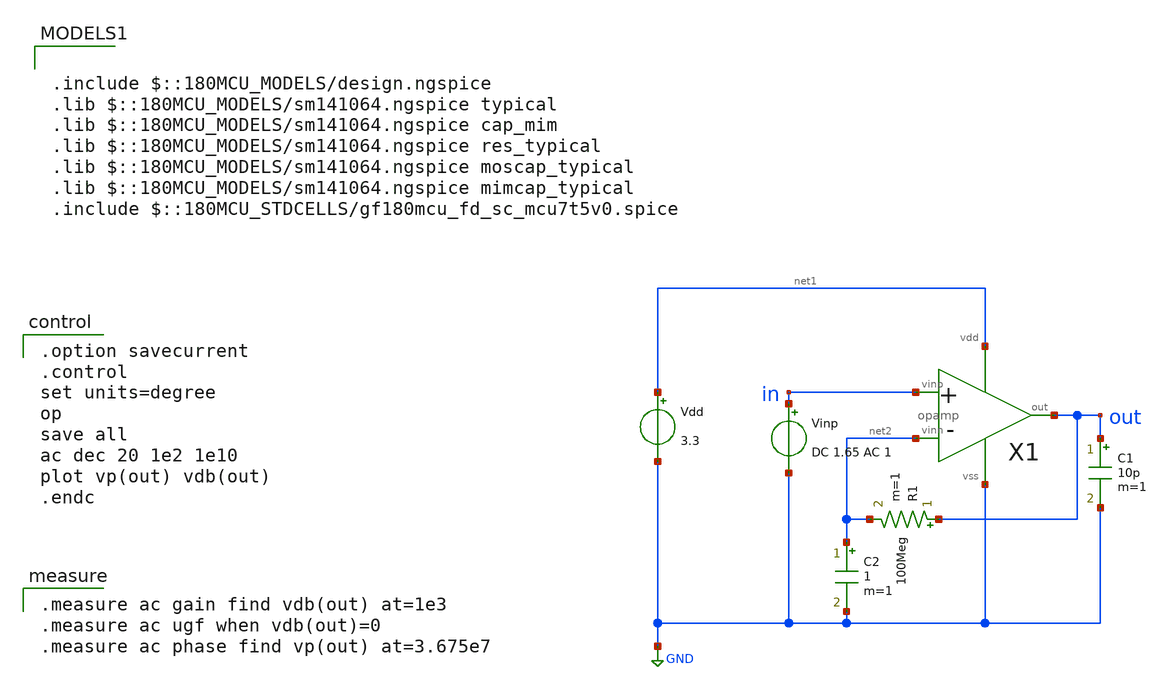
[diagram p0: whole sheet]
** sch_path: opamp_ac.sch
**.subckt opamp_ac
Vdd net1 GND 3.3
Vinp in GND DC 1.65 AC 1
X1 in net2 out net1 GND opamp
R1 out net2 100Meg m=1
C2 net2 GND 1 m=1
C1 out GND 10p m=1
**** begin user architecture code

.option savecurrent
.control
set units=degree
op
save all
ac dec 20 1e2 1e10
plot vp(out) vdb(out)
.endc


.measure ac gain find vdb(out) at=1e3
.measure ac ugf when vdb(out)=0
.measure ac phase find vp(out) at=3.675e7


.include $::180MCU_MODELS/design.ngspice
.lib $::180MCU_MODELS/sm141064.ngspice typical
.lib $::180MCU_MODELS/sm141064.ngspice cap_mim
.lib $::180MCU_MODELS/sm141064.ngspice res_typical
.lib $::180MCU_MODELS/sm141064.ngspice moscap_typical
.lib $::180MCU_MODELS/sm141064.ngspice mimcap_typical
.include $::180MCU_STDCELLS/gf180mcu_fd_sc_mcu7t5v0.spice

**** end user architecture code
**.ends

* expanding   symbol:  opamp.sym # of pins=5
** sym_path: opamp.sym
** sch_path: opamp.sch
.subckt opamp vinp vinn out vdd vss
*.opin out
*.iopin vdd
*.iopin vss
*.ipin vinp
*.ipin vinn
XM2 net2 net1 vdd vdd pfet_03v3 L=0.6u W=6.0u nf=1 ad='int((nf+1)/2) * W/nf * 0.18u' as='int((nf+2)/2) * W/nf * 0.18u'
+ pd='2*int((nf+1)/2) * (W/nf + 0.18u)' ps='2*int((nf+2)/2) * (W/nf + 0.18u)' nrd='0.18u / W' nrs='0.18u / W'
+ sa=0 sb=0 sd=0 m=1
XM3 net1 net3 net2 vdd pfet_03v3 L=0.6u W=6.0u nf=1 ad='int((nf+1)/2) * W/nf * 0.18u' as='int((nf+2)/2) * W/nf * 0.18u'
+ pd='2*int((nf+1)/2) * (W/nf + 0.18u)' ps='2*int((nf+2)/2) * (W/nf + 0.18u)' nrd='0.18u / W' nrs='0.18u / W'
+ sa=0 sb=0 sd=0 m=1
XM1 net3 net3 vdd vdd pfet_03v3 L=0.6u W=1.2u nf=1 ad='int((nf+1)/2) * W/nf * 0.18u' as='int((nf+2)/2) * W/nf * 0.18u'
+ pd='2*int((nf+1)/2) * (W/nf + 0.18u)' ps='2*int((nf+2)/2) * (W/nf + 0.18u)' nrd='0.18u / W' nrs='0.18u / W'
+ sa=0 sb=0 sd=0 m=1
XM9 net8 net7 net4 vss nfet_03v3 L=0.6u W=3.0u nf=1 ad='int((nf+1)/2) * W/nf * 0.18u' as='int((nf+2)/2) * W/nf * 0.18u'
+ pd='2*int((nf+1)/2) * (W/nf + 0.18u)' ps='2*int((nf+2)/2) * (W/nf + 0.18u)' nrd='0.18u / W' nrs='0.18u / W'
+ sa=0 sb=0 sd=0 m=1
XM10 net4 net8 vss vss nfet_03v3 L=0.6u W=3.0u nf=1 ad='int((nf+1)/2) * W/nf * 0.18u' as='int((nf+2)/2) * W/nf * 0.18u'
+ pd='2*int((nf+1)/2) * (W/nf + 0.18u)' ps='2*int((nf+2)/2) * (W/nf + 0.18u)' nrd='0.18u / W' nrs='0.18u / W'
+ sa=0 sb=0 sd=0 m=1
XM6 net7 net7 vss vss nfet_03v3 L=0.6u W=0.6u nf=1 ad='int((nf+1)/2) * W/nf * 0.18u' as='int((nf+2)/2) * W/nf * 0.18u'
+ pd='2*int((nf+1)/2) * (W/nf + 0.18u)' ps='2*int((nf+2)/2) * (W/nf + 0.18u)' nrd='0.18u / W' nrs='0.18u / W'
+ sa=0 sb=0 sd=0 m=1
I3 net3 vss 8u
I1 net1 vss 8u
C1 out net13 440f m=1
C2 net14 out 440f m=1
XM4 net6 net1 vdd vdd pfet_03v3 L=0.6u W=6.0u nf=1 ad='int((nf+1)/2) * W/nf * 0.18u' as='int((nf+2)/2) * W/nf * 0.18u'
+ pd='2*int((nf+1)/2) * (W/nf + 0.18u)' ps='2*int((nf+2)/2) * (W/nf + 0.18u)' nrd='0.18u / W' nrs='0.18u / W'
+ sa=0 sb=0 sd=0 m=1
XM5 net7 net3 net6 vdd pfet_03v3 L=0.6u W=6.0u nf=1 ad='int((nf+1)/2) * W/nf * 0.18u' as='int((nf+2)/2) * W/nf * 0.18u'
+ pd='2*int((nf+1)/2) * (W/nf + 0.18u)' ps='2*int((nf+2)/2) * (W/nf + 0.18u)' nrd='0.18u / W' nrs='0.18u / W'
+ sa=0 sb=0 sd=0 m=1
XM7 net5 net1 vdd vdd pfet_03v3 L=0.6u W=6.0u nf=1 ad='int((nf+1)/2) * W/nf * 0.18u' as='int((nf+2)/2) * W/nf * 0.18u'
+ pd='2*int((nf+1)/2) * (W/nf + 0.18u)' ps='2*int((nf+2)/2) * (W/nf + 0.18u)' nrd='0.18u / W' nrs='0.18u / W'
+ sa=0 sb=0 sd=0 m=1
XM8 net8 net3 net5 vdd pfet_03v3 L=0.6u W=6.0u nf=1 ad='int((nf+1)/2) * W/nf * 0.18u' as='int((nf+2)/2) * W/nf * 0.18u'
+ pd='2*int((nf+1)/2) * (W/nf + 0.18u)' ps='2*int((nf+2)/2) * (W/nf + 0.18u)' nrd='0.18u / W' nrs='0.18u / W'
+ sa=0 sb=0 sd=0 m=1
XM25 net12 net18 vss vss nfet_03v3 L=0.6u W=6.0u nf=1 ad='int((nf+1)/2) * W/nf * 0.18u' as='int((nf+2)/2) * W/nf * 0.18u'
+ pd='2*int((nf+1)/2) * (W/nf + 0.18u)' ps='2*int((nf+2)/2) * (W/nf + 0.18u)' nrd='0.18u / W' nrs='0.18u / W'
+ sa=0 sb=0 sd=0 m=1
XM27 net17 net19 net18 vss nfet_03v3 L=0.6u W=1.5u nf=1 ad='int((nf+1)/2) * W/nf * 0.18u' as='int((nf+2)/2) * W/nf * 0.18u'
+ pd='2*int((nf+1)/2) * (W/nf + 0.18u)' ps='2*int((nf+2)/2) * (W/nf + 0.18u)' nrd='0.18u / W' nrs='0.18u / W'
+ sa=0 sb=0 sd=0 m=1
XM28 net20 net19 net30 vss nfet_03v3 L=0.6u W=1.5u nf=1 ad='int((nf+1)/2) * W/nf * 0.18u' as='int((nf+2)/2) * W/nf * 0.18u'
+ pd='2*int((nf+1)/2) * (W/nf + 0.18u)' ps='2*int((nf+2)/2) * (W/nf + 0.18u)' nrd='0.18u / W' nrs='0.18u / W'
+ sa=0 sb=0 sd=0 m=1
XM32 net30 net29 net20 vdd pfet_03v3 L=0.6u W=3.0u nf=1 ad='int((nf+1)/2) * W/nf * 0.18u' as='int((nf+2)/2) * W/nf * 0.18u'
+ pd='2*int((nf+1)/2) * (W/nf + 0.18u)' ps='2*int((nf+2)/2) * (W/nf + 0.18u)' nrd='0.18u / W' nrs='0.18u / W'
+ sa=0 sb=0 sd=0 m=1
XM33 net18 net29 net17 vdd pfet_03v3 L=0.6u W=3.0u nf=1 ad='int((nf+1)/2) * W/nf * 0.18u' as='int((nf+2)/2) * W/nf * 0.18u'
+ pd='2*int((nf+1)/2) * (W/nf + 0.18u)' ps='2*int((nf+2)/2) * (W/nf + 0.18u)' nrd='0.18u / W' nrs='0.18u / W'
+ sa=0 sb=0 sd=0 m=1
XM11 net27 net1 vdd vdd pfet_03v3 L=0.6u W=6.0u nf=1 ad='int((nf+1)/2) * W/nf * 0.18u' as='int((nf+2)/2) * W/nf * 0.18u'
+ pd='2*int((nf+1)/2) * (W/nf + 0.18u)' ps='2*int((nf+2)/2) * (W/nf + 0.18u)' nrd='0.18u / W' nrs='0.18u / W'
+ sa=0 sb=0 sd=0 m=1
XM12 net15 net3 net27 vdd pfet_03v3 L=0.6u W=6.0u nf=1 ad='int((nf+1)/2) * W/nf * 0.18u' as='int((nf+2)/2) * W/nf * 0.18u'
+ pd='2*int((nf+1)/2) * (W/nf + 0.18u)' ps='2*int((nf+2)/2) * (W/nf + 0.18u)' nrd='0.18u / W' nrs='0.18u / W'
+ sa=0 sb=0 sd=0 m=1
XM13 net10 net1 vdd vdd pfet_03v3 L=0.6u W=6.0u nf=1 ad='int((nf+1)/2) * W/nf * 0.18u' as='int((nf+2)/2) * W/nf * 0.18u'
+ pd='2*int((nf+1)/2) * (W/nf + 0.18u)' ps='2*int((nf+2)/2) * (W/nf + 0.18u)' nrd='0.18u / W' nrs='0.18u / W'
+ sa=0 sb=0 sd=0 m=1
XM14 net15 net3 net10 vdd pfet_03v3 L=0.6u W=6.0u nf=1 ad='int((nf+1)/2) * W/nf * 0.18u' as='int((nf+2)/2) * W/nf * 0.18u'
+ pd='2*int((nf+1)/2) * (W/nf + 0.18u)' ps='2*int((nf+2)/2) * (W/nf + 0.18u)' nrd='0.18u / W' nrs='0.18u / W'
+ sa=0 sb=0 sd=0 m=1
XM15 net12 vinn net15 vdd pfet_03v3 L=0.6u W=6.0u nf=1 ad='int((nf+1)/2) * W/nf * 0.18u' as='int((nf+2)/2) * W/nf * 0.18u'
+ pd='2*int((nf+1)/2) * (W/nf + 0.18u)' ps='2*int((nf+2)/2) * (W/nf + 0.18u)' nrd='0.18u / W' nrs='0.18u / W'
+ sa=0 sb=0 sd=0 m=1
XM16 net13 vinp net15 vdd pfet_03v3 L=0.6u W=6.0u nf=1 ad='int((nf+1)/2) * W/nf * 0.18u' as='int((nf+2)/2) * W/nf * 0.18u'
+ pd='2*int((nf+1)/2) * (W/nf + 0.18u)' ps='2*int((nf+2)/2) * (W/nf + 0.18u)' nrd='0.18u / W' nrs='0.18u / W'
+ sa=0 sb=0 sd=0 m=1
XM17 net16 net7 net28 vss nfet_03v3 L=0.6u W=3.0u nf=1 ad='int((nf+1)/2) * W/nf * 0.18u' as='int((nf+2)/2) * W/nf * 0.18u'
+ pd='2*int((nf+1)/2) * (W/nf + 0.18u)' ps='2*int((nf+2)/2) * (W/nf + 0.18u)' nrd='0.18u / W' nrs='0.18u / W'
+ sa=0 sb=0 sd=0 m=1
XM18 net28 net8 vss vss nfet_03v3 L=0.6u W=3.0u nf=1 ad='int((nf+1)/2) * W/nf * 0.18u' as='int((nf+2)/2) * W/nf * 0.18u'
+ pd='2*int((nf+1)/2) * (W/nf + 0.18u)' ps='2*int((nf+2)/2) * (W/nf + 0.18u)' nrd='0.18u / W' nrs='0.18u / W'
+ sa=0 sb=0 sd=0 m=1
XM19 net16 net7 net9 vss nfet_03v3 L=0.6u W=3.0u nf=1 ad='int((nf+1)/2) * W/nf * 0.18u' as='int((nf+2)/2) * W/nf * 0.18u'
+ pd='2*int((nf+1)/2) * (W/nf + 0.18u)' ps='2*int((nf+2)/2) * (W/nf + 0.18u)' nrd='0.18u / W' nrs='0.18u / W'
+ sa=0 sb=0 sd=0 m=1
XM20 net9 net8 vss vss nfet_03v3 L=0.6u W=3.0u nf=1 ad='int((nf+1)/2) * W/nf * 0.18u' as='int((nf+2)/2) * W/nf * 0.18u'
+ pd='2*int((nf+1)/2) * (W/nf + 0.18u)' ps='2*int((nf+2)/2) * (W/nf + 0.18u)' nrd='0.18u / W' nrs='0.18u / W'
+ sa=0 sb=0 sd=0 m=1
XM21 net11 vinn net16 vss nfet_03v3 L=0.6u W=3.0u nf=1 ad='int((nf+1)/2) * W/nf * 0.18u' as='int((nf+2)/2) * W/nf * 0.18u'
+ pd='2*int((nf+1)/2) * (W/nf + 0.18u)' ps='2*int((nf+2)/2) * (W/nf + 0.18u)' nrd='0.18u / W' nrs='0.18u / W'
+ sa=0 sb=0 sd=0 m=1
XM22 net14 vinp net16 vss nfet_03v3 L=0.6u W=3.0u nf=1 ad='int((nf+1)/2) * W/nf * 0.18u' as='int((nf+2)/2) * W/nf * 0.18u'
+ pd='2*int((nf+1)/2) * (W/nf + 0.18u)' ps='2*int((nf+2)/2) * (W/nf + 0.18u)' nrd='0.18u / W' nrs='0.18u / W'
+ sa=0 sb=0 sd=0 m=1
XM23 net18 net7 net12 vss nfet_03v3 L=0.6u W=3.0u nf=1 ad='int((nf+1)/2) * W/nf * 0.18u' as='int((nf+2)/2) * W/nf * 0.18u'
+ pd='2*int((nf+1)/2) * (W/nf + 0.18u)' ps='2*int((nf+2)/2) * (W/nf + 0.18u)' nrd='0.18u / W' nrs='0.18u / W'
+ sa=0 sb=0 sd=0 m=1
XM24 net30 net7 net13 vss nfet_03v3 L=0.6u W=3.0u nf=1 ad='int((nf+1)/2) * W/nf * 0.18u' as='int((nf+2)/2) * W/nf * 0.18u'
+ pd='2*int((nf+1)/2) * (W/nf + 0.18u)' ps='2*int((nf+2)/2) * (W/nf + 0.18u)' nrd='0.18u / W' nrs='0.18u / W'
+ sa=0 sb=0 sd=0 m=1
XM29 net17 net3 net11 vdd pfet_03v3 L=0.6u W=6.0u nf=1 ad='int((nf+1)/2) * W/nf * 0.18u' as='int((nf+2)/2) * W/nf * 0.18u'
+ pd='2*int((nf+1)/2) * (W/nf + 0.18u)' ps='2*int((nf+2)/2) * (W/nf + 0.18u)' nrd='0.18u / W' nrs='0.18u / W'
+ sa=0 sb=0 sd=0 m=1
XM30 net20 net3 net14 vdd pfet_03v3 L=0.6u W=6.0u nf=1 ad='int((nf+1)/2) * W/nf * 0.18u' as='int((nf+2)/2) * W/nf * 0.18u'
+ pd='2*int((nf+1)/2) * (W/nf + 0.18u)' ps='2*int((nf+2)/2) * (W/nf + 0.18u)' nrd='0.18u / W' nrs='0.18u / W'
+ sa=0 sb=0 sd=0 m=1
XM31 net11 net17 vdd vdd pfet_03v3 L=0.6u W=12.0u nf=1 ad='int((nf+1)/2) * W/nf * 0.18u' as='int((nf+2)/2) * W/nf * 0.18u'
+ pd='2*int((nf+1)/2) * (W/nf + 0.18u)' ps='2*int((nf+2)/2) * (W/nf + 0.18u)' nrd='0.18u / W' nrs='0.18u / W'
+ sa=0 sb=0 sd=0 m=1
XM35 net14 net17 vdd vdd pfet_03v3 L=0.6u W=12.0u nf=1 ad='int((nf+1)/2) * W/nf * 0.18u' as='int((nf+2)/2) * W/nf * 0.18u'
+ pd='2*int((nf+1)/2) * (W/nf + 0.18u)' ps='2*int((nf+2)/2) * (W/nf + 0.18u)' nrd='0.18u / W' nrs='0.18u / W'
+ sa=0 sb=0 sd=0 m=1
XM34 net22 net3 net21 vdd pfet_03v3 L=0.6u W=6.0u nf=1 ad='int((nf+1)/2) * W/nf * 0.18u' as='int((nf+2)/2) * W/nf * 0.18u'
+ pd='2*int((nf+1)/2) * (W/nf + 0.18u)' ps='2*int((nf+2)/2) * (W/nf + 0.18u)' nrd='0.18u / W' nrs='0.18u / W'
+ sa=0 sb=0 sd=0 m=1
XM36 net21 net22 vdd vdd pfet_03v3 L=0.6u W=6.0u nf=1 ad='int((nf+1)/2) * W/nf * 0.18u' as='int((nf+2)/2) * W/nf * 0.18u'
+ pd='2*int((nf+1)/2) * (W/nf + 0.18u)' ps='2*int((nf+2)/2) * (W/nf + 0.18u)' nrd='0.18u / W' nrs='0.18u / W'
+ sa=0 sb=0 sd=0 m=1
XM37 net29 net29 net22 vdd pfet_03v3 L=0.6u W=6.0u nf=1 ad='int((nf+1)/2) * W/nf * 0.18u' as='int((nf+2)/2) * W/nf * 0.18u'
+ pd='2*int((nf+1)/2) * (W/nf + 0.18u)' ps='2*int((nf+2)/2) * (W/nf + 0.18u)' nrd='0.18u / W' nrs='0.18u / W'
+ sa=0 sb=0 sd=0 m=1
XM45 net19 net3 net24 vdd pfet_03v3 L=0.6u W=6.0u nf=1 ad='int((nf+1)/2) * W/nf * 0.18u' as='int((nf+2)/2) * W/nf * 0.18u'
+ pd='2*int((nf+1)/2) * (W/nf + 0.18u)' ps='2*int((nf+2)/2) * (W/nf + 0.18u)' nrd='0.18u / W' nrs='0.18u / W'
+ sa=0 sb=0 sd=0 m=1
XM46 net24 net1 vdd vdd pfet_03v3 L=0.6u W=6.0u nf=1 ad='int((nf+1)/2) * W/nf * 0.18u' as='int((nf+2)/2) * W/nf * 0.18u'
+ pd='2*int((nf+1)/2) * (W/nf + 0.18u)' ps='2*int((nf+2)/2) * (W/nf + 0.18u)' nrd='0.18u / W' nrs='0.18u / W'
+ sa=0 sb=0 sd=0 m=1
XM38 net29 net7 net23 vss nfet_03v3 L=0.6u W=3.0u nf=1 ad='int((nf+1)/2) * W/nf * 0.18u' as='int((nf+2)/2) * W/nf * 0.18u'
+ pd='2*int((nf+1)/2) * (W/nf + 0.18u)' ps='2*int((nf+2)/2) * (W/nf + 0.18u)' nrd='0.18u / W' nrs='0.18u / W'
+ sa=0 sb=0 sd=0 m=1
XM39 net23 net8 vss vss nfet_03v3 L=0.6u W=3.0u nf=1 ad='int((nf+1)/2) * W/nf * 0.18u' as='int((nf+2)/2) * W/nf * 0.18u'
+ pd='2*int((nf+1)/2) * (W/nf + 0.18u)' ps='2*int((nf+2)/2) * (W/nf + 0.18u)' nrd='0.18u / W' nrs='0.18u / W'
+ sa=0 sb=0 sd=0 m=1
XM40 net19 net19 net26 vss nfet_03v3 L=0.6u W=3.0u nf=1 ad='int((nf+1)/2) * W/nf * 0.18u' as='int((nf+2)/2) * W/nf * 0.18u'
+ pd='2*int((nf+1)/2) * (W/nf + 0.18u)' ps='2*int((nf+2)/2) * (W/nf + 0.18u)' nrd='0.18u / W' nrs='0.18u / W'
+ sa=0 sb=0 sd=0 m=1
XM41 net26 net7 net25 vss nfet_03v3 L=0.6u W=3.0u nf=1 ad='int((nf+1)/2) * W/nf * 0.18u' as='int((nf+2)/2) * W/nf * 0.18u'
+ pd='2*int((nf+1)/2) * (W/nf + 0.18u)' ps='2*int((nf+2)/2) * (W/nf + 0.18u)' nrd='0.18u / W' nrs='0.18u / W'
+ sa=0 sb=0 sd=0 m=1
XM42 net25 net26 vss vss nfet_03v3 L=0.6u W=3.0u nf=1 ad='int((nf+1)/2) * W/nf * 0.18u' as='int((nf+2)/2) * W/nf * 0.18u'
+ pd='2*int((nf+1)/2) * (W/nf + 0.18u)' ps='2*int((nf+2)/2) * (W/nf + 0.18u)' nrd='0.18u / W' nrs='0.18u / W'
+ sa=0 sb=0 sd=0 m=1
XM43 out net30 vss vss nfet_03v3 L=0.6u W=15.0u nf=1 ad='int((nf+1)/2) * W/nf * 0.18u' as='int((nf+2)/2) * W/nf * 0.18u'
+ pd='2*int((nf+1)/2) * (W/nf + 0.18u)' ps='2*int((nf+2)/2) * (W/nf + 0.18u)' nrd='0.18u / W' nrs='0.18u / W'
+ sa=0 sb=0 sd=0 m=1
XM44 out net20 vdd vdd pfet_03v3 L=0.6u W=30.0u nf=1 ad='int((nf+1)/2) * W/nf * 0.18u' as='int((nf+2)/2) * W/nf * 0.18u'
+ pd='2*int((nf+1)/2) * (W/nf + 0.18u)' ps='2*int((nf+2)/2) * (W/nf + 0.18u)' nrd='0.18u / W' nrs='0.18u / W'
+ sa=0 sb=0 sd=0 m=1
XM26 net13 net18 vss vss nfet_03v3 L=0.6u W=6.0u nf=1 ad='int((nf+1)/2) * W/nf * 0.18u' as='int((nf+2)/2) * W/nf * 0.18u'
+ pd='2*int((nf+1)/2) * (W/nf + 0.18u)' ps='2*int((nf+2)/2) * (W/nf + 0.18u)' nrd='0.18u / W' nrs='0.18u / W'
+ sa=0 sb=0 sd=0 m=1
.ends

.GLOBAL GND
.end
